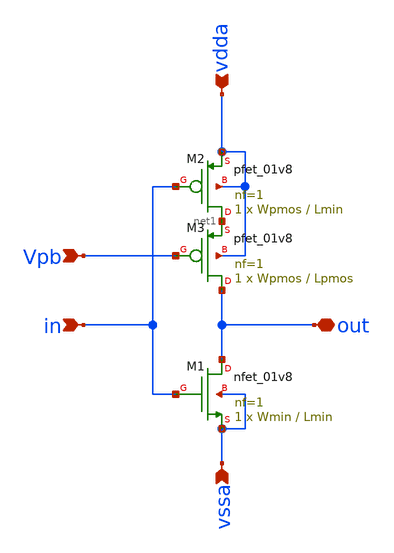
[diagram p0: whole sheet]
** sch_path: xschem/inv/inv_weak_pullup.sch
**.subckt inv_weak_pullup in out Vpb vdda vssa
*.ipin in
*.iopin out
*.ipin Vpb
*.ipin vdda
*.ipin vssa
XM1 out in vssa vssa sky130_fd_pr__nfet_01v8 L=Lmin W=Wmin nf=1 ad='int((nf+1)/2) * W/nf * 0.29' as='int((nf+2)/2) * W/nf * 0.29'
+ pd='2*int((nf+1)/2) * (W/nf + 0.29)' ps='2*int((nf+2)/2) * (W/nf + 0.29)' nrd='0.29 / W' nrs='0.29 / W'
+ sa=0 sb=0 sd=0 mult=1 m=1
XM2 net1 in vdda vdda sky130_fd_pr__pfet_01v8 L=Lmin W=Wpmos nf=1 ad='int((nf+1)/2) * W/nf * 0.29' as='int((nf+2)/2) * W/nf * 0.29'
+ pd='2*int((nf+1)/2) * (W/nf + 0.29)' ps='2*int((nf+2)/2) * (W/nf + 0.29)' nrd='0.29 / W' nrs='0.29 / W'
+ sa=0 sb=0 sd=0 mult=1 m=1
XM3 out Vpb net1 vdda sky130_fd_pr__pfet_01v8 L=Lpmos W=Wpmos nf=1 ad='int((nf+1)/2) * W/nf * 0.29' as='int((nf+2)/2) * W/nf * 0.29'
+ pd='2*int((nf+1)/2) * (W/nf + 0.29)' ps='2*int((nf+2)/2) * (W/nf + 0.29)' nrd='0.29 / W' nrs='0.29 / W'
+ sa=0 sb=0 sd=0 mult=1 m=1
**.ends
.end
